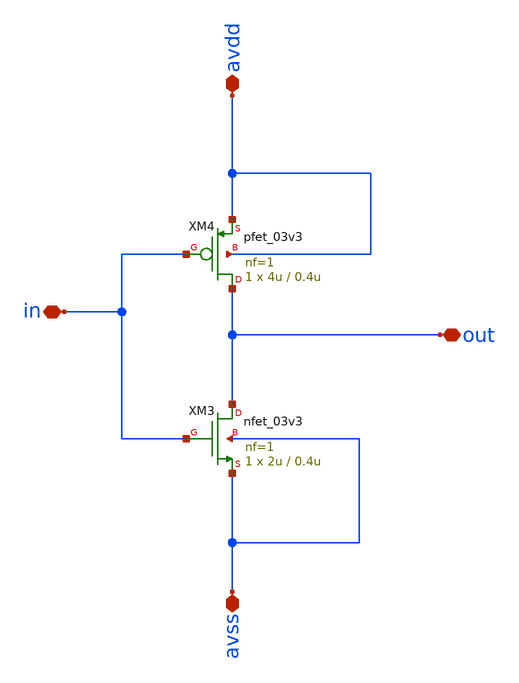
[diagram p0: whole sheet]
** sch_path: designs/comparator/final_magic/osu_sc/inverter/mia/inv_mia.sch
**.subckt inv_mia avdd avss in out
*.iopin avdd
*.iopin avss
*.iopin in
*.iopin out
XM3 out in avss avss nfet_03v3 L=0.4u W=2u nf=1 ad='int((nf+1)/2) * W/nf * 0.18u' as='int((nf+2)/2) * W/nf * 0.18u'
+ pd='2*int((nf+1)/2) * (W/nf + 0.18u)' ps='2*int((nf+2)/2) * (W/nf + 0.18u)' nrd='0.18u / W' nrs='0.18u / W'
+ sa=0 sb=0 sd=0 m=1
XM4 out in avdd avdd pfet_03v3 L=0.4u W=4u nf=1 ad='int((nf+1)/2) * W/nf * 0.18u' as='int((nf+2)/2) * W/nf * 0.18u'
+ pd='2*int((nf+1)/2) * (W/nf + 0.18u)' ps='2*int((nf+2)/2) * (W/nf + 0.18u)' nrd='0.18u / W' nrs='0.18u / W'
+ sa=0 sb=0 sd=0 m=1
**.ends
.end
